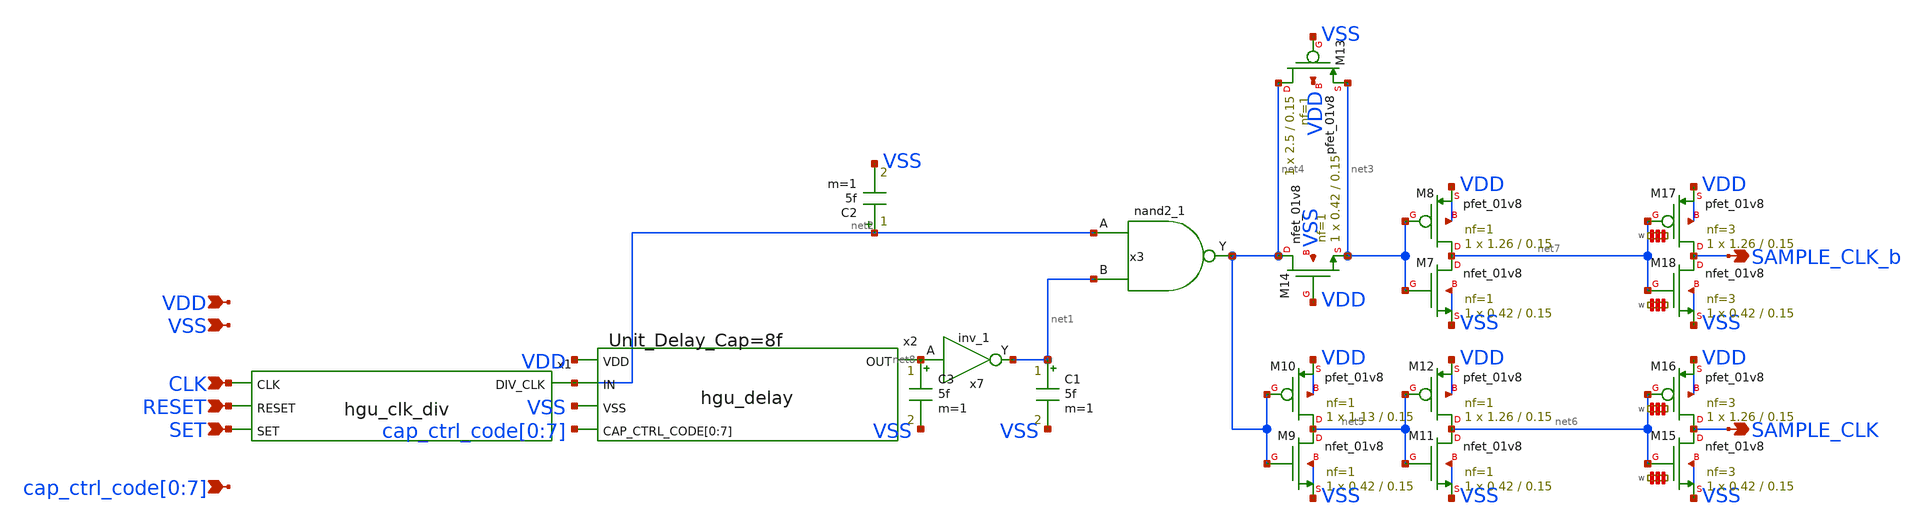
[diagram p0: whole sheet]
** sch_path: hgu/xschem/hgu_clk_sample.sch
**.subckt hgu_clk_sample VDD VSS SET RESET CLK
*+ cap_ctrl_code[0],cap_ctrl_code[1],cap_ctrl_code[2],cap_ctrl_code[3],cap_ctrl_code[4],cap_ctrl_code[5],cap_ctrl_code[6],cap_ctrl_code[7] SAMPLE_CLK SAMPLE_CLK_b
*.ipin VDD
*.ipin VSS
*.ipin SET
*.ipin RESET
*.ipin CLK
*.ipin
*+ cap_ctrl_code[0],cap_ctrl_code[1],cap_ctrl_code[2],cap_ctrl_code[3],cap_ctrl_code[4],cap_ctrl_code[5],cap_ctrl_code[6],cap_ctrl_code[7]
*.opin SAMPLE_CLK
*.opin SAMPLE_CLK_b
x1 net2 CLK RESET SET hgu_clk_div
x2 VDD net2 net8 VSS cap_ctrl_code[0] cap_ctrl_code[1] cap_ctrl_code[2] cap_ctrl_code[3]
+ cap_ctrl_code[4] cap_ctrl_code[5] cap_ctrl_code[6] cap_ctrl_code[7] hgu_delay DELAY_CAP=8f
x7 net8 VGND VNB VPB VPWR net1 sky130_fd_sc_hd__inv_1
C1 net1 VSS 5f m=1
C2 net2 VSS 5f m=1
C3 net8 VSS 5f m=1
x3 net2 net1 VGND VNB VPB VPWR net4 sky130_fd_sc_hd__nand2_1
XM7 net7 net3 VSS VSS sky130_fd_pr__nfet_01v8 L=0.15 W=0.42 nf=1 ad='int((nf+1)/2) * W/nf * 0.29' as='int((nf+2)/2) * W/nf * 0.29'
+ pd='2*int((nf+1)/2) * (W/nf + 0.29)' ps='2*int((nf+2)/2) * (W/nf + 0.29)' nrd='0.29 / W' nrs='0.29 / W'
+ sa=0 sb=0 sd=0 mult=1 m=1
XM8 net7 net3 VDD VDD sky130_fd_pr__pfet_01v8 L=0.15 W=1.26 nf=1 ad='int((nf+1)/2) * W/nf * 0.29' as='int((nf+2)/2) * W/nf * 0.29'
+ pd='2*int((nf+1)/2) * (W/nf + 0.29)' ps='2*int((nf+2)/2) * (W/nf + 0.29)' nrd='0.29 / W' nrs='0.29 / W'
+ sa=0 sb=0 sd=0 mult=1 m=1
XM9 net5 net4 VSS VSS sky130_fd_pr__nfet_01v8 L=0.15 W=0.42 nf=1 ad='int((nf+1)/2) * W/nf * 0.29' as='int((nf+2)/2) * W/nf * 0.29'
+ pd='2*int((nf+1)/2) * (W/nf + 0.29)' ps='2*int((nf+2)/2) * (W/nf + 0.29)' nrd='0.29 / W' nrs='0.29 / W'
+ sa=0 sb=0 sd=0 mult=1 m=1
XM10 net5 net4 VDD VDD sky130_fd_pr__pfet_01v8 L=0.15 W=1.13 nf=1 ad='int((nf+1)/2) * W/nf * 0.29' as='int((nf+2)/2) * W/nf * 0.29'
+ pd='2*int((nf+1)/2) * (W/nf + 0.29)' ps='2*int((nf+2)/2) * (W/nf + 0.29)' nrd='0.29 / W' nrs='0.29 / W'
+ sa=0 sb=0 sd=0 mult=1 m=1
XM11 net6 net5 VSS VSS sky130_fd_pr__nfet_01v8 L=0.15 W=0.42 nf=1 ad='int((nf+1)/2) * W/nf * 0.29' as='int((nf+2)/2) * W/nf * 0.29'
+ pd='2*int((nf+1)/2) * (W/nf + 0.29)' ps='2*int((nf+2)/2) * (W/nf + 0.29)' nrd='0.29 / W' nrs='0.29 / W'
+ sa=0 sb=0 sd=0 mult=1 m=1
XM12 net6 net5 VDD VDD sky130_fd_pr__pfet_01v8 L=0.15 W=1.26 nf=1 ad='int((nf+1)/2) * W/nf * 0.29' as='int((nf+2)/2) * W/nf * 0.29'
+ pd='2*int((nf+1)/2) * (W/nf + 0.29)' ps='2*int((nf+2)/2) * (W/nf + 0.29)' nrd='0.29 / W' nrs='0.29 / W'
+ sa=0 sb=0 sd=0 mult=1 m=1
XM13 net4 VSS net3 VDD sky130_fd_pr__pfet_01v8 L=0.15 W=2.5 nf=1 ad='int((nf+1)/2) * W/nf * 0.29' as='int((nf+2)/2) * W/nf * 0.29'
+ pd='2*int((nf+1)/2) * (W/nf + 0.29)' ps='2*int((nf+2)/2) * (W/nf + 0.29)' nrd='0.29 / W' nrs='0.29 / W'
+ sa=0 sb=0 sd=0 mult=1 m=1
XM14 net4 VDD net3 VSS sky130_fd_pr__nfet_01v8 L=0.15 W=0.42 nf=1 ad='int((nf+1)/2) * W/nf * 0.29' as='int((nf+2)/2) * W/nf * 0.29'
+ pd='2*int((nf+1)/2) * (W/nf + 0.29)' ps='2*int((nf+2)/2) * (W/nf + 0.29)' nrd='0.29 / W' nrs='0.29 / W'
+ sa=0 sb=0 sd=0 mult=1 m=1
XM15 SAMPLE_CLK net6 VSS VSS sky130_fd_pr__nfet_01v8 L=0.15 W='0.42 * 3 ' nf=3 ad='int((nf+1)/2) * W / nf * 0.29'
+ as='int((nf+2)/2) * W / nf * 0.29' pd='2*int((nf+1)/2) * (W / nf + 0.29)' ps='2*int((nf+2)/2) * (W / nf + 0.29)'
+ nrd='0.29 / W ' nrs='0.29 / W ' sa=0 sb=0 sd=0 mult=1 m=1
XM16 SAMPLE_CLK net6 VDD VDD sky130_fd_pr__pfet_01v8 L=0.15 W='1.26 * 3 ' nf=3 ad='int((nf+1)/2) * W / nf * 0.29'
+ as='int((nf+2)/2) * W / nf * 0.29' pd='2*int((nf+1)/2) * (W / nf + 0.29)' ps='2*int((nf+2)/2) * (W / nf + 0.29)'
+ nrd='0.29 / W ' nrs='0.29 / W ' sa=0 sb=0 sd=0 mult=1 m=1
XM17 SAMPLE_CLK_b net7 VDD VDD sky130_fd_pr__pfet_01v8 L=0.15 W='1.26 * 3 ' nf=3 ad='int((nf+1)/2) * W / nf * 0.29'
+ as='int((nf+2)/2) * W / nf * 0.29' pd='2*int((nf+1)/2) * (W / nf + 0.29)' ps='2*int((nf+2)/2) * (W / nf + 0.29)'
+ nrd='0.29 / W ' nrs='0.29 / W ' sa=0 sb=0 sd=0 mult=1 m=1
XM18 SAMPLE_CLK_b net7 VSS VSS sky130_fd_pr__nfet_01v8 L=0.15 W='0.42 * 3 ' nf=3 ad='int((nf+1)/2) * W / nf * 0.29'
+ as='int((nf+2)/2) * W / nf * 0.29' pd='2*int((nf+1)/2) * (W / nf + 0.29)' ps='2*int((nf+2)/2) * (W / nf + 0.29)'
+ nrd='0.29 / W ' nrs='0.29 / W ' sa=0 sb=0 sd=0 mult=1 m=1
**.ends
.end
